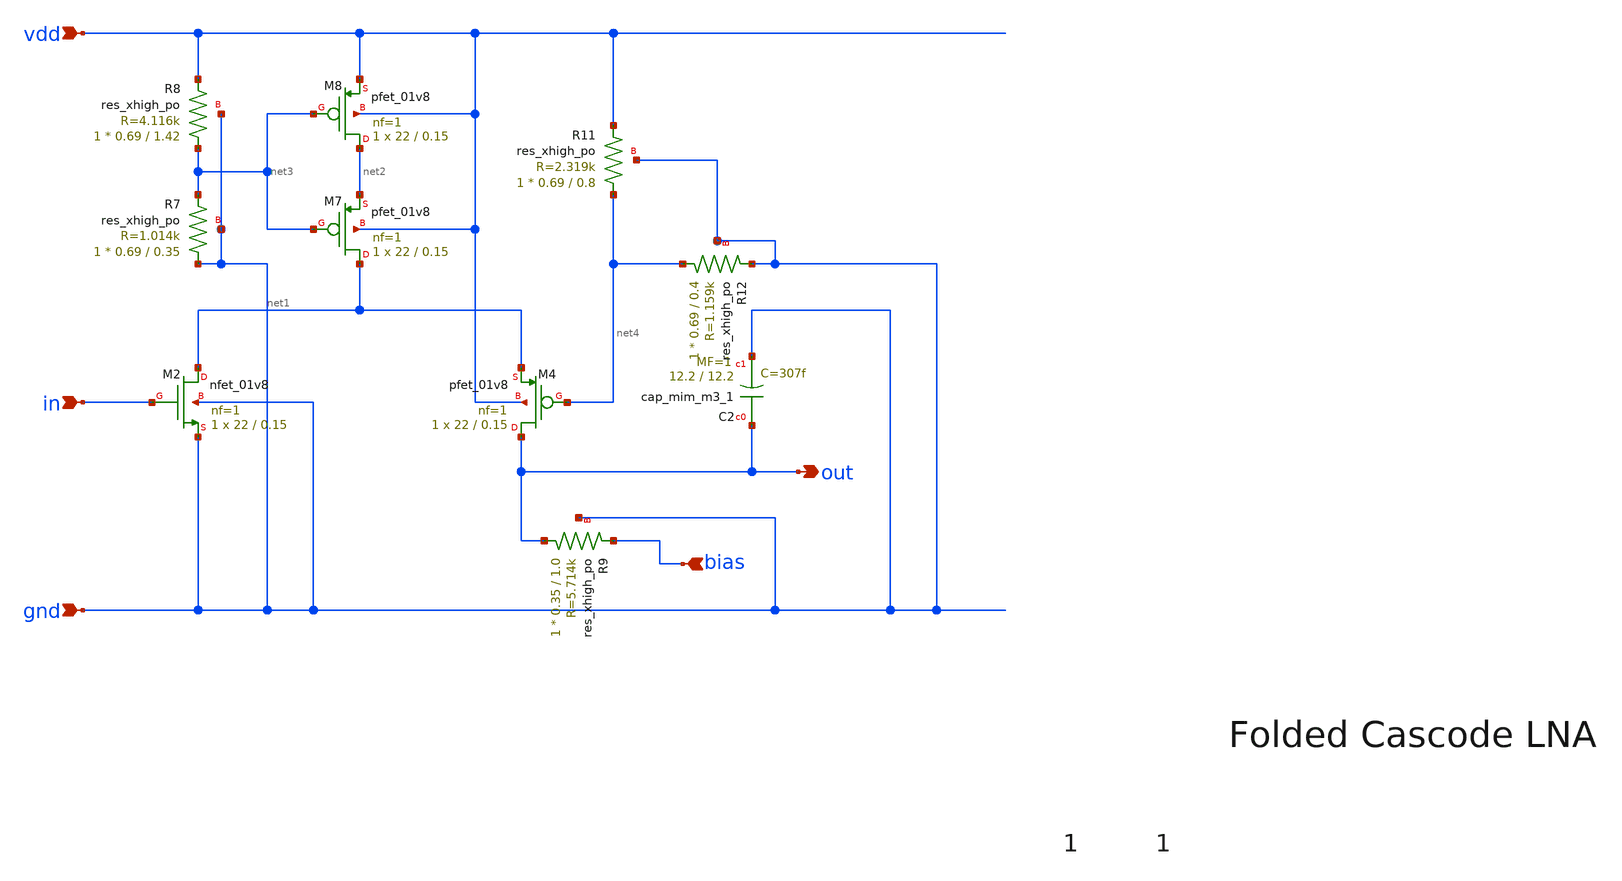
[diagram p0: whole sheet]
** sch_path: xschem/lna/foldedcascode.sch
**.subckt foldedcascode out vdd gnd in bias
*.opin out
*.ipin vdd
*.ipin gnd
*.ipin in
*.ipin bias
XM2 net1 in gnd gnd sky130_fd_pr__nfet_01v8 L=0.15 W=22 nf=1 ad='int((nf+1)/2) * W/nf * 0.29' as='int((nf+2)/2) * W/nf * 0.29'
+ pd='2*int((nf+1)/2) * (W/nf + 0.29)' ps='2*int((nf+2)/2) * (W/nf + 0.29)' nrd='0.29 / W' nrs='0.29 / W'
+ sa=0 sb=0 sd=0 mult=1 m=1
XM4 out net4 net1 vdd sky130_fd_pr__pfet_01v8 L=0.15 W=22 nf=1 ad='int((nf+1)/2) * W/nf * 0.29' as='int((nf+2)/2) * W/nf * 0.29'
+ pd='2*int((nf+1)/2) * (W/nf + 0.29)' ps='2*int((nf+2)/2) * (W/nf + 0.29)' nrd='0.29 / W' nrs='0.29 / W'
+ sa=0 sb=0 sd=0 mult=1 m=1
XM7 net1 net3 net2 vdd sky130_fd_pr__pfet_01v8 L=0.15 W=22 nf=1 ad='int((nf+1)/2) * W/nf * 0.29' as='int((nf+2)/2) * W/nf * 0.29'
+ pd='2*int((nf+1)/2) * (W/nf + 0.29)' ps='2*int((nf+2)/2) * (W/nf + 0.29)' nrd='0.29 / W' nrs='0.29 / W'
+ sa=0 sb=0 sd=0 mult=1 m=1
XM8 net2 net3 vdd vdd sky130_fd_pr__pfet_01v8 L=0.15 W=22 nf=1 ad='int((nf+1)/2) * W/nf * 0.29' as='int((nf+2)/2) * W/nf * 0.29'
+ pd='2*int((nf+1)/2) * (W/nf + 0.29)' ps='2*int((nf+2)/2) * (W/nf + 0.29)' nrd='0.29 / W' nrs='0.29 / W'
+ sa=0 sb=0 sd=0 mult=1 m=1
XR7 gnd net3 gnd sky130_fd_pr__res_xhigh_po W=0.69 L=0.35 mult=1 m=1
XR8 net3 vdd gnd sky130_fd_pr__res_xhigh_po W=0.69 L=1.42 mult=1 m=1
XR9 out bias gnd sky130_fd_pr__res_xhigh_po W=0.35 L=1.0 mult=1 m=1
XC2 out gnd sky130_fd_pr__cap_mim_m3_1 W=12.2 L=12.2 MF=1 m=1
XR11 net4 vdd gnd sky130_fd_pr__res_xhigh_po W=0.69 L=0.8 mult=1 m=1
XR12 net4 gnd gnd sky130_fd_pr__res_xhigh_po W=0.69 L=0.4 mult=1 m=1
**** begin user architecture code
 ** manual skywater pdks install (with patches applied)
* .lib $::SKYWATER_MODELS/models/sky130.lib.spice tt

** opencircuitdesign pdks install
.lib /foss/pdk/sky130A/libs.tech/ngspice/sky130.lib.spice tt

.param mc_mm_switch=0
.param mc_pr_switch=0

**** end user architecture code
**.ends
.end
